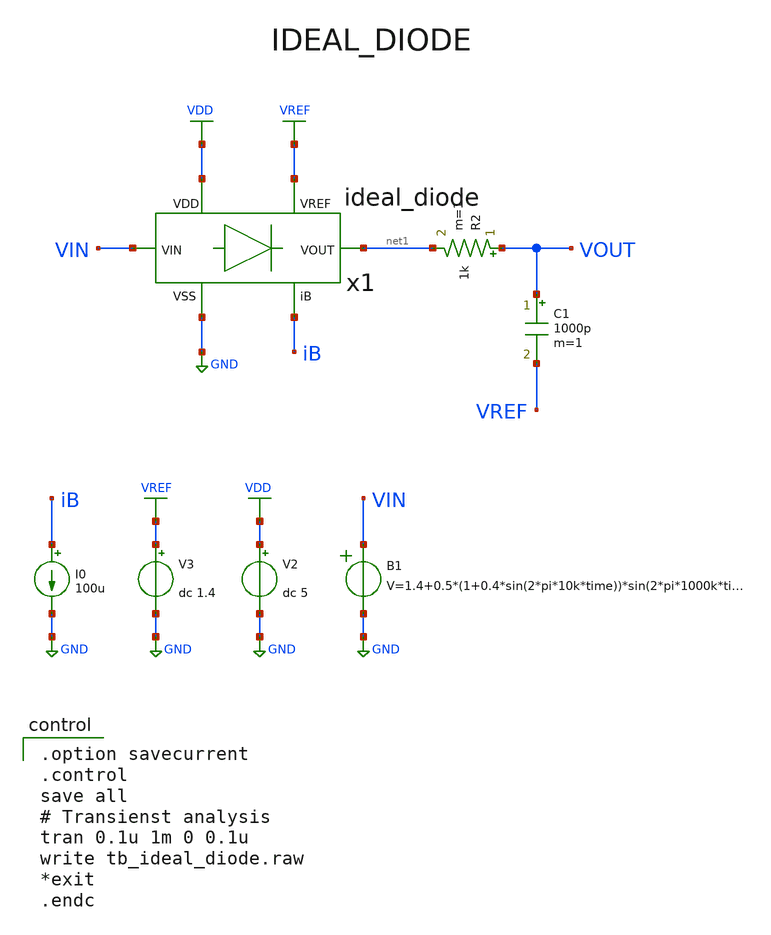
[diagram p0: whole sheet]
** sch_path: member_project/AM_Radio/Yamada3/xschem/tb_ideal_diode.sch
**.subckt tb_ideal_diode
V2 VDD GND dc 5
V3 VREF GND dc 1.4
B1 VIN GND V=1.4+0.5*(1+0.4*sin(2*pi*10k*time))*sin(2*pi*1000k*time)
R2 VOUT net1 1k m=1
x1 VDD GND VIN net1 iB VREF ideal_diode
I0 iB GND 100u
C1 VOUT VREF 1000p m=1
**** begin user architecture code
 .include $::LIB/ip62_models

.option savecurrent
.control
save all
# Transienst analysis
tran 0.1u 1m 0 0.1u
write tb_ideal_diode.raw
*exit
.endc

**** end user architecture code
**.ends

* expanding   symbol:  ideal_diode.sym # of pins=6
** sym_path: member_project/AM_Radio/Yamada3/xschem/ideal_diode.sym
** sch_path: member_project/AM_Radio/Yamada3/xschem/ideal_diode.sch
.subckt ideal_diode VDD VSS VIN VOUT iB VREF
*.iopin VDD
*.ipin VIN
*.opin VOUT
*.iopin VSS
*.iopin VREF
*.iopin iB
XR1 VOUT VREF VDD F_RR w=4e-06 R=20k l=76.9e-06 tc1=0 tc2=0
x1 VDD net1 VIN VOUT opout iB net2 cascode_opamp_2
XXC1 VOUT opout VSS F_CSIO c=540f x=30u y=30u m=1
DD1 opout VOUT DP m=4
DD2 VREF opout DP m=4
.ends


* expanding   symbol:  cascode_opamp_2.sym # of pins=7
** sym_path: member_project/AM_Radio/noritsuna/xschem/cascode_opamp_2.sym
** sch_path: member_project/AM_Radio/noritsuna/xschem/cascode_opamp_2.sch
.subckt cascode_opamp_2 VDD VSS VIN_P VIN_N VOUT VB2 VB1
*.opin VOUT
*.ipin VIN_N
*.ipin VIN_P
*.ipin VSS
*.ipin VDD
*.ipin VB1
*.ipin VB2
MM2 net2 net1 VDD VDD PMOS w=240u l=8u as=0 ad=0 ps=0 pd=0 nrd=0 nrs=0 m=1
MM4 OUT1 VB2 MN_MDMY4 VSS NMOS w=84u l=8u as=0 ad=0 ps=0 pd=0 nrd=0 nrs=0 m=1
MM7 VOUT iB VDD VDD PMOS w=2400u l=8u as=0 ad=0 ps=0 pd=0 nrd=0 nrs=0 m=1
MM8 VOUT OUT1 VSS VSS NMOS w=1680u l=8u as=0 ad=0 ps=0 pd=0 nrd=0 nrs=0 m=1
MM16 net1 net1 VDD VDD PMOS w=240u l=8u as=0 ad=0 ps=0 pd=0 nrd=0 nrs=0 m=1
MM17 OUT1 MPN_MDMY3 net2 VDD PMOS w=240u l=8u as=0 ad=0 ps=0 pd=0 nrd=0 nrs=0 m=1
MM18 MPN_MDMY3 MPN_MDMY3 net1 VDD PMOS w=240u l=8u as=0 ad=0 ps=0 pd=0 nrd=0 nrs=0 m=1
MM19 MPN_MDMY3 VB2 MN_MDMY2 VSS NMOS w=84u l=8u as=0 ad=0 ps=0 pd=0 nrd=0 nrs=0 m=1
MM20 MN_MDMY4 VIN_P MN_MDMY5 VSS NMOS w=672u l=8u as=0 ad=0 ps=0 pd=0 nrd=0 nrs=0 m=1
MM21 MN_MDMY2 VIN_N MN_MDMY5 VSS NMOS w=672u l=8u as=0 ad=0 ps=0 pd=0 nrd=0 nrs=0 m=1
MM22 MN_MDMY5 VB1 VSS VSS NMOS w=84u l=8u as=0 ad=0 ps=0 pd=0 nrd=0 nrs=0 m=1
MM3 net3 net7 OUT1 VSS NMOS w=168u l=8u as=0 ad=0 ps=0 pd=0 nrd=0 nrs=0 m=1
MM6 net4 net4 VSS VSS NMOS w=168u l=8u as=0 ad=0 ps=0 pd=0 nrd=0 nrs=0 m=1
MM13 VB2 VB2 VB1 VSS NMOS w=84u l=8u as=0 ad=0 ps=0 pd=0 nrd=0 nrs=0 m=1
MM14 VB1 VB1 VSS VSS NMOS w=84u l=8u as=0 ad=0 ps=0 pd=0 nrd=0 nrs=0 m=1
MM23 VB4 VB4 VDD VDD PMOS w=240u l=8u as=0 ad=0 ps=0 pd=0 nrd=0 nrs=0 m=1
MM24 VB2 iB net5 VDD PMOS w=240u l=8u as=0 ad=0 ps=0 pd=0 nrd=0 nrs=0 m=1
MM25 net5 VB4 VDD VDD PMOS w=240u l=8u as=0 ad=0 ps=0 pd=0 nrd=0 nrs=0 m=1
MM26 iB iB VB4 VDD PMOS w=240u l=8u as=0 ad=0 ps=0 pd=0 nrd=0 nrs=0 m=1
MM1 net7 iB net6 VDD PMOS w=240u l=8u as=0 ad=0 ps=0 pd=0 nrd=0 nrs=0 m=1
MM9 net6 VB4 VDD VDD PMOS w=240u l=8u as=0 ad=0 ps=0 pd=0 nrd=0 nrs=0 m=1
MM5 net7 net7 net4 VSS NMOS w=168u l=8u as=0 ad=0 ps=0 pd=0 nrd=0 nrs=0 m=1
XXC1 net3 VOUT VSS F_CSIO c=540f x=30u y=30u m=1
XMDMYN2 MN_MDMY2 VSS VSS VSS NMOS w=42u l=8u as=0 ad=0 ps=0 pd=0 nrd=0 nrs=0 m=2
XMDMYN3 MPN_MDMY3 VSS VSS VSS NMOS w=7u l=8u as=0 ad=0 ps=0 pd=0 nrd=0 nrs=0 m=4
XMDMYN4 MN_MDMY4 VSS VSS VSS NMOS w=42u l=8u as=0 ad=0 ps=0 pd=0 nrd=0 nrs=0 m=2
XMDMYN5 MN_MDMY5 VSS VSS VSS NMOS w=42u l=8u as=0 ad=0 ps=0 pd=0 nrd=0 nrs=0 m=2
XMDMYN6 OUT1 VSS VSS VSS NMOS w=42u l=8u as=0 ad=0 ps=0 pd=0 nrd=0 nrs=0 m=4
XMDMYP1 iB VDD VDD VDD PMOS w=20u l=8u as=0 ad=0 ps=0 pd=0 nrd=0 nrs=0 m=4
XMDMYP2 MPN_MDMY3 VDD VDD VDD PMOS w=20u l=8u as=0 ad=0 ps=0 pd=0 nrd=0 nrs=0 m=4
XMDMYP3 VDD VDD VDD VDD PMOS w=60u l=8u as=0 ad=0 ps=0 pd=0 nrd=0 nrs=0 m=4
MM10 iB VB2 net8 VSS NMOS w=84u l=8u as=0 ad=0 ps=0 pd=0 nrd=0 nrs=0 m=1
MM11 net8 VB1 VSS VSS NMOS w=84u l=8u as=0 ad=0 ps=0 pd=0 nrd=0 nrs=0 m=1
XMDMYN7 iB VSS VSS VSS NMOS w=7u l=8u as=0 ad=0 ps=0 pd=0 nrd=0 nrs=0 m=4
.ends

.GLOBAL GND
.GLOBAL VDD
.GLOBAL VREF
.end
